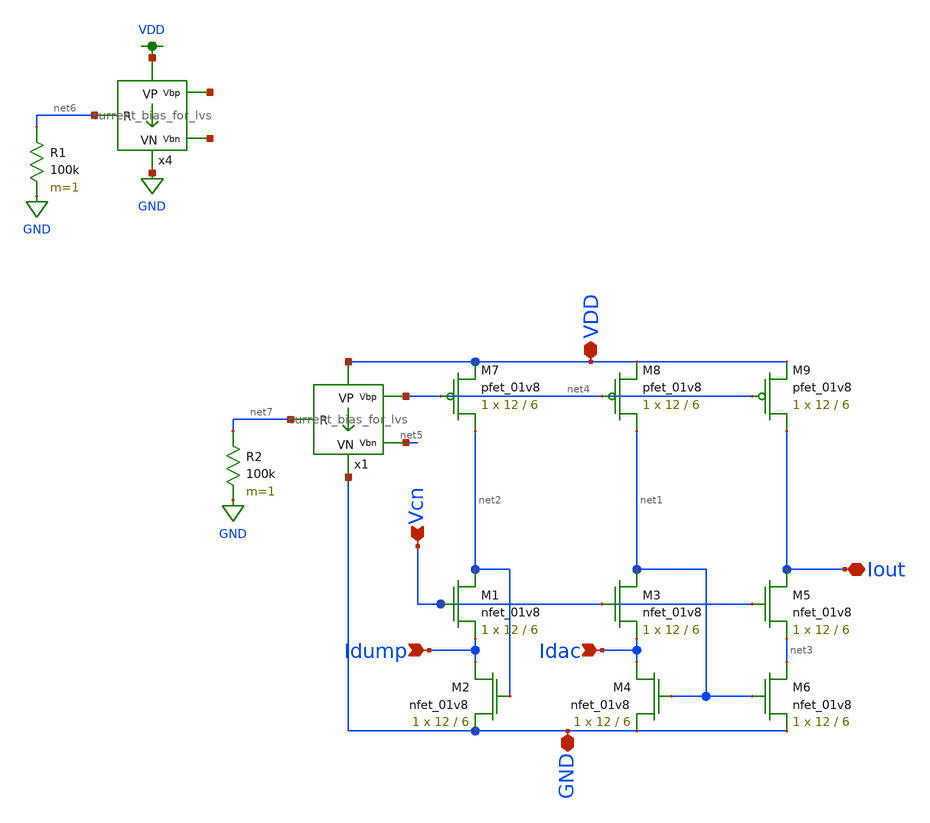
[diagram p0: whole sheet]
** sch_path: schematics/ieee DAC/Output_stage.sch
**.subckt Output_stage VDD GND Idac Idump Iout Vcn
*.iopin VDD
*.iopin GND
*.ipin Idac
*.ipin Idump
*.iopin Iout
*.ipin Vcn
XM1 net2 Vcn Idump GND sky130_fd_pr__nfet_01v8 L=6 W=12 nf=1 ad='int((nf+1)/2) * W/nf * 0.29' as='int((nf+2)/2) * W/nf * 0.29'
+ pd='2*int((nf+1)/2) * (W/nf + 0.29)' ps='2*int((nf+2)/2) * (W/nf + 0.29)' nrd='0.29 / W' nrs='0.29 / W'
+ sa=0 sb=0 sd=0 mult=1 m=1
XM2 Idump net2 GND GND sky130_fd_pr__nfet_01v8 L=6 W=12 nf=1 ad='int((nf+1)/2) * W/nf * 0.29' as='int((nf+2)/2) * W/nf * 0.29'
+ pd='2*int((nf+1)/2) * (W/nf + 0.29)' ps='2*int((nf+2)/2) * (W/nf + 0.29)' nrd='0.29 / W' nrs='0.29 / W'
+ sa=0 sb=0 sd=0 mult=1 m=1
XM3 net1 Vcn Idac GND sky130_fd_pr__nfet_01v8 L=6 W=12 nf=1 ad='int((nf+1)/2) * W/nf * 0.29' as='int((nf+2)/2) * W/nf * 0.29'
+ pd='2*int((nf+1)/2) * (W/nf + 0.29)' ps='2*int((nf+2)/2) * (W/nf + 0.29)' nrd='0.29 / W' nrs='0.29 / W'
+ sa=0 sb=0 sd=0 mult=1 m=1
XM4 Idac net1 GND GND sky130_fd_pr__nfet_01v8 L=6 W=12 nf=1 ad='int((nf+1)/2) * W/nf * 0.29' as='int((nf+2)/2) * W/nf * 0.29'
+ pd='2*int((nf+1)/2) * (W/nf + 0.29)' ps='2*int((nf+2)/2) * (W/nf + 0.29)' nrd='0.29 / W' nrs='0.29 / W'
+ sa=0 sb=0 sd=0 mult=1 m=1
XM5 Iout Vcn net3 GND sky130_fd_pr__nfet_01v8 L=6 W=12 nf=1 ad='int((nf+1)/2) * W/nf * 0.29' as='int((nf+2)/2) * W/nf * 0.29'
+ pd='2*int((nf+1)/2) * (W/nf + 0.29)' ps='2*int((nf+2)/2) * (W/nf + 0.29)' nrd='0.29 / W' nrs='0.29 / W'
+ sa=0 sb=0 sd=0 mult=1 m=1
XM6 net3 net1 GND GND sky130_fd_pr__nfet_01v8 L=6 W=12 nf=1 ad='int((nf+1)/2) * W/nf * 0.29' as='int((nf+2)/2) * W/nf * 0.29'
+ pd='2*int((nf+1)/2) * (W/nf + 0.29)' ps='2*int((nf+2)/2) * (W/nf + 0.29)' nrd='0.29 / W' nrs='0.29 / W'
+ sa=0 sb=0 sd=0 mult=1 m=1
XM7 net2 net4 VDD VDD sky130_fd_pr__pfet_01v8 L=6 W=12 nf=1 ad='int((nf+1)/2) * W/nf * 0.29' as='int((nf+2)/2) * W/nf * 0.29'
+ pd='2*int((nf+1)/2) * (W/nf + 0.29)' ps='2*int((nf+2)/2) * (W/nf + 0.29)' nrd='0.29 / W' nrs='0.29 / W'
+ sa=0 sb=0 sd=0 mult=1 m=1
XM8 net1 net4 VDD VDD sky130_fd_pr__pfet_01v8 L=6 W=12 nf=1 ad='int((nf+1)/2) * W/nf * 0.29' as='int((nf+2)/2) * W/nf * 0.29'
+ pd='2*int((nf+1)/2) * (W/nf + 0.29)' ps='2*int((nf+2)/2) * (W/nf + 0.29)' nrd='0.29 / W' nrs='0.29 / W'
+ sa=0 sb=0 sd=0 mult=1 m=1
XM9 Iout net4 VDD VDD sky130_fd_pr__pfet_01v8 L=6 W=12 nf=1 ad='int((nf+1)/2) * W/nf * 0.29' as='int((nf+2)/2) * W/nf * 0.29'
+ pd='2*int((nf+1)/2) * (W/nf + 0.29)' ps='2*int((nf+2)/2) * (W/nf + 0.29)' nrd='0.29 / W' nrs='0.29 / W'
+ sa=0 sb=0 sd=0 mult=1 m=1
R1 net6 GND 100k m=1
x4 VDD GND net8 net9 net6 current_bias_for_lvs
R2 net7 GND 100k m=1
x1 VDD GND net4 net5 net7 current_bias_for_lvs
**.ends
.GLOBAL GND
.GLOBAL VDD
.end
